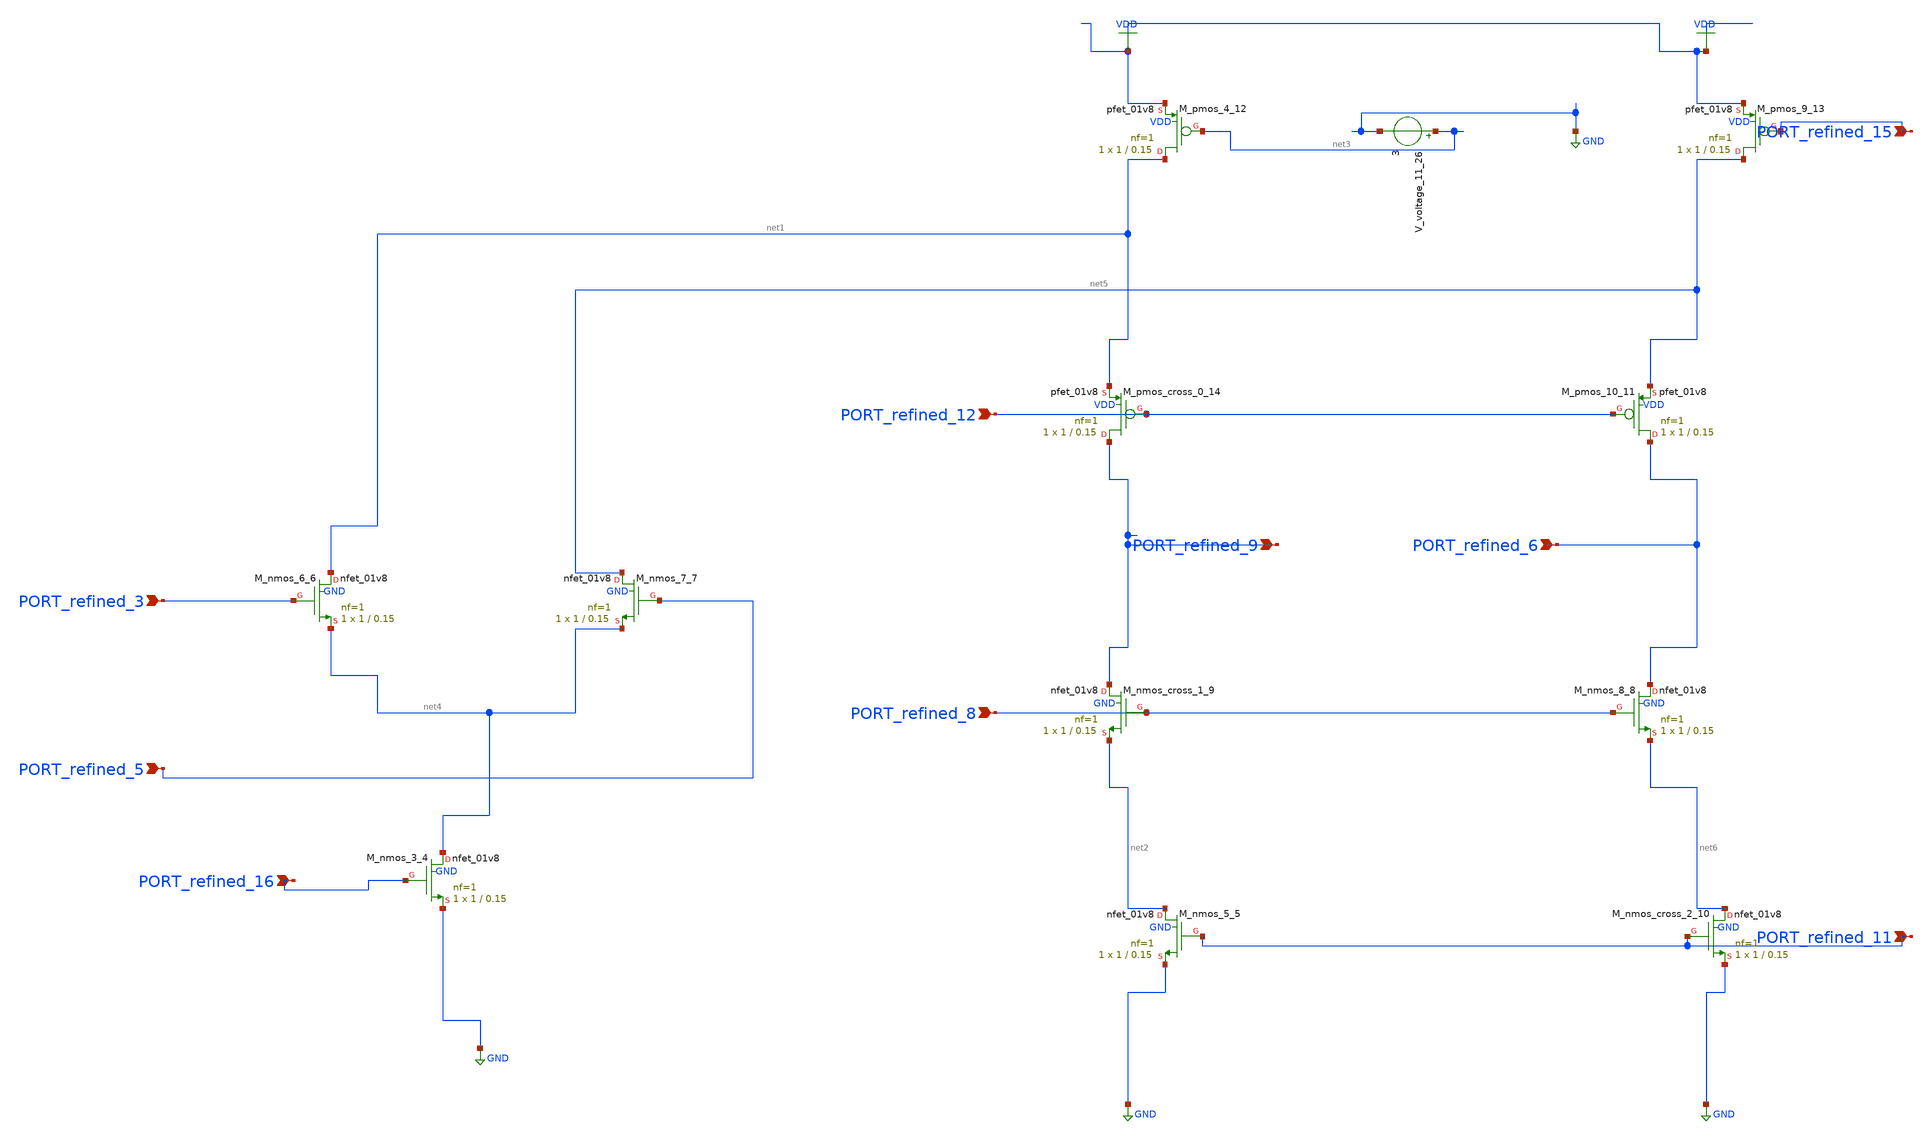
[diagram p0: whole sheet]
** sch_path: schematics/AMSNet/710.sch
**.subckt 710 PORT_refined_12 PORT_refined_8 PORT_refined_11 PORT_refined_5 PORT_refined_3
*+ PORT_refined_16 PORT_refined_9 PORT_refined_6 PORT_refined_15
*.ipin PORT_refined_12
*.ipin PORT_refined_8
*.ipin PORT_refined_11
*.ipin PORT_refined_5
*.ipin PORT_refined_3
*.ipin PORT_refined_16
*.ipin PORT_refined_9
*.ipin PORT_refined_6
*.ipin PORT_refined_15
XM_nmos_3_4 net4 PORT_refined_16 GND GND sky130_fd_pr__nfet_01v8 L=0.15 W=1 nf=1 ad='int((1 + 1)/2) * 1 / 1 * 0.29'
+ as='int((1 + 2)/2) * 1 / 1 * 0.29' pd='2*int((1 + 1)/2) * (1 / 1 + 0.29)' ps='2*int((1 + 2)/2) * (1 / 1 + 0.29)'
+ nrd='0.29 / 1 ' nrs='0.29 / 1 ' sa=0 sb=0 sd=0 mult=1 m=1
XM_nmos_5_5 net2 PORT_refined_11 GND GND sky130_fd_pr__nfet_01v8 L=0.15 W=1 nf=1 ad='int((1 + 1)/2) * 1 / 1 * 0.29'
+ as='int((1 + 2)/2) * 1 / 1 * 0.29' pd='2*int((1 + 1)/2) * (1 / 1 + 0.29)' ps='2*int((1 + 2)/2) * (1 / 1 + 0.29)'
+ nrd='0.29 / 1 ' nrs='0.29 / 1 ' sa=0 sb=0 sd=0 mult=1 m=1
XM_nmos_6_6 net1 PORT_refined_3 net4 GND sky130_fd_pr__nfet_01v8 L=0.15 W=1 nf=1 ad='int((1 + 1)/2) * 1 / 1 * 0.29'
+ as='int((1 + 2)/2) * 1 / 1 * 0.29' pd='2*int((1 + 1)/2) * (1 / 1 + 0.29)' ps='2*int((1 + 2)/2) * (1 / 1 + 0.29)'
+ nrd='0.29 / 1 ' nrs='0.29 / 1 ' sa=0 sb=0 sd=0 mult=1 m=1
XM_nmos_7_7 net5 PORT_refined_5 net4 GND sky130_fd_pr__nfet_01v8 L=0.15 W=1 nf=1 ad='int((1 + 1)/2) * 1 / 1 * 0.29'
+ as='int((1 + 2)/2) * 1 / 1 * 0.29' pd='2*int((1 + 1)/2) * (1 / 1 + 0.29)' ps='2*int((1 + 2)/2) * (1 / 1 + 0.29)'
+ nrd='0.29 / 1 ' nrs='0.29 / 1 ' sa=0 sb=0 sd=0 mult=1 m=1
XM_nmos_8_8 PORT_refined_6 PORT_refined_8 net6 GND sky130_fd_pr__nfet_01v8 L=0.15 W=1 nf=1 ad='int((1 + 1)/2) * 1 / 1 * 0.29'
+ as='int((1 + 2)/2) * 1 / 1 * 0.29' pd='2*int((1 + 1)/2) * (1 / 1 + 0.29)' ps='2*int((1 + 2)/2) * (1 / 1 + 0.29)'
+ nrd='0.29 / 1 ' nrs='0.29 / 1 ' sa=0 sb=0 sd=0 mult=1 m=1
XM_nmos_cross_1_9 PORT_refined_9 PORT_refined_8 net2 GND sky130_fd_pr__nfet_01v8 L=0.15 W=1 nf=1 ad='int((1 + 1)/2) * 1 / 1 * 0.29'
+ as='int((1 + 2)/2) * 1 / 1 * 0.29' pd='2*int((1 + 1)/2) * (1 / 1 + 0.29)' ps='2*int((1 + 2)/2) * (1 / 1 + 0.29)'
+ nrd='0.29 / 1 ' nrs='0.29 / 1 ' sa=0 sb=0 sd=0 mult=1 m=1
XM_nmos_cross_2_10 net6 PORT_refined_11 GND GND sky130_fd_pr__nfet_01v8 L=0.15 W=1 nf=1 ad='int((1 + 1)/2) * 1 / 1 * 0.29'
+ as='int((1 + 2)/2) * 1 / 1 * 0.29' pd='2*int((1 + 1)/2) * (1 / 1 + 0.29)' ps='2*int((1 + 2)/2) * (1 / 1 + 0.29)'
+ nrd='0.29 / 1 ' nrs='0.29 / 1 ' sa=0 sb=0 sd=0 mult=1 m=1
XM_pmos_10_11 PORT_refined_6 PORT_refined_12 net5 VDD sky130_fd_pr__pfet_01v8 L=0.15 W=1 nf=1 ad='int((1 + 1)/2) * 1 / 1 * 0.29'
+ as='int((1 + 2)/2) * 1 / 1 * 0.29' pd='2*int((1 + 1)/2) * (1 / 1 + 0.29)' ps='2*int((1 + 2)/2) * (1 / 1 + 0.29)'
+ nrd='0.29 / 1 ' nrs='0.29 / 1 ' sa=0 sb=0 sd=0 mult=1 m=1
XM_pmos_4_12 net1 net3 VDD VDD sky130_fd_pr__pfet_01v8 L=0.15 W=1 nf=1 ad='int((1 + 1)/2) * 1 / 1 * 0.29'
+ as='int((1 + 2)/2) * 1 / 1 * 0.29' pd='2*int((1 + 1)/2) * (1 / 1 + 0.29)' ps='2*int((1 + 2)/2) * (1 / 1 + 0.29)'
+ nrd='0.29 / 1 ' nrs='0.29 / 1 ' sa=0 sb=0 sd=0 mult=1 m=1
XM_pmos_9_13 net5 PORT_refined_15 VDD VDD sky130_fd_pr__pfet_01v8 L=0.15 W=1 nf=1 ad='int((1 + 1)/2) * 1 / 1 * 0.29'
+ as='int((1 + 2)/2) * 1 / 1 * 0.29' pd='2*int((1 + 1)/2) * (1 / 1 + 0.29)' ps='2*int((1 + 2)/2) * (1 / 1 + 0.29)'
+ nrd='0.29 / 1 ' nrs='0.29 / 1 ' sa=0 sb=0 sd=0 mult=1 m=1
XM_pmos_cross_0_14 PORT_refined_9 PORT_refined_12 net1 VDD sky130_fd_pr__pfet_01v8 L=0.15 W=1 nf=1 ad='int((1 + 1)/2) * 1 / 1 * 0.29'
+ as='int((1 + 2)/2) * 1 / 1 * 0.29' pd='2*int((1 + 1)/2) * (1 / 1 + 0.29)' ps='2*int((1 + 2)/2) * (1 / 1 + 0.29)'
+ nrd='0.29 / 1 ' nrs='0.29 / 1 ' sa=0 sb=0 sd=0 mult=1 m=1
V_voltage_11_26 net3 GND 3
**.ends
.GLOBAL GND
.GLOBAL VDD
.end
